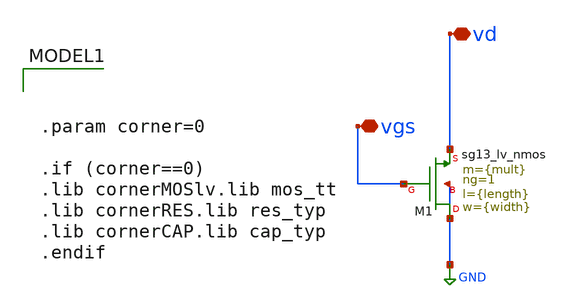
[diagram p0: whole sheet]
** sch_path: Tarea_1/xschem/W_id-vs-gm_id.sch
**.subckt W_id-vs-gm_id vgs vd
*.iopin vgs
*.iopin vd
XM1 GND vgs vd GND sg13_lv_nmos w={width} l={length} ng=1 m={mult} mm_ok=1
**** begin user architecture code


.param corner=0

.if (corner==0)
.lib cornerMOSlv.lib mos_tt
.lib cornerRES.lib res_typ
.lib cornerCAP.lib cap_typ
.endif



.option wnflag=1

.param length= 0.26u
.param width = 1u
.param mult = 1


vin vgs 0 0.520
vds vd 0 1.2

.control

shell rm -f gmid_sweep_w.raw

save all
save @n.xm1.nsg13_lv_nmos[gm]
save @n.xm1.nsg13_lv_nmos[ids]

dc vds 0.01 1.8 0.01
let idn  = @n.xm1.nsg13_lv_nmos[ids]
let gmn  = @n.xm1.nsg13_lv_nmos[gm]

let gmid = gmn/idn
let idw  = idn/1u
wrdata gmid_sweep_w.raw gmid idw
.endc



**** end user architecture code
**.ends
.GLOBAL GND
.end
